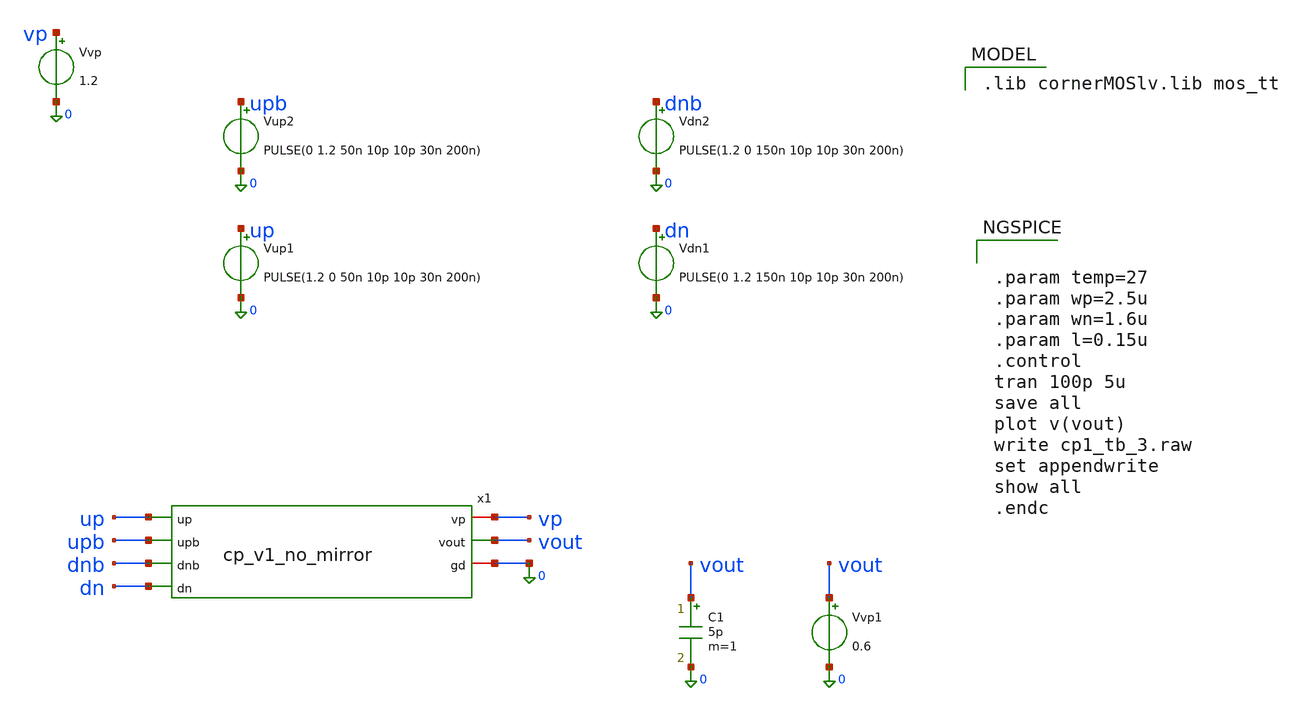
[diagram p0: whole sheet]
** sch_path: charge_pump/cp_v1_tb.sch
**.subckt cp_v1_tb
Vvp vp 0 1.2
Vup1 up 0 PULSE(1.2 0 50n 10p 10p 30n 200n)
Vdn1 dn 0 PULSE(0 1.2 150n 10p 10p 30n 200n)
C1 vout 0 5p m=1
Vup2 upb 0 PULSE(0 1.2 50n 10p 10p 30n 200n)
Vdn2 dnb 0 PULSE(1.2 0 150n 10p 10p 30n 200n)
x1 vp up upb vout dnb dn 0 cp_v1_no_mirror
Vvp1 vout 0 0.6
**** begin user architecture code
 .lib cornerMOSlv.lib mos_tt



.param temp=27
.param wp=2.5u
.param wn=1.6u
.param l=0.15u
.control
tran 100p 5u
save all
plot v(vout)
write cp1_tb_3.raw
set appendwrite
show all
.endc


**** end user architecture code
**.ends
.end
